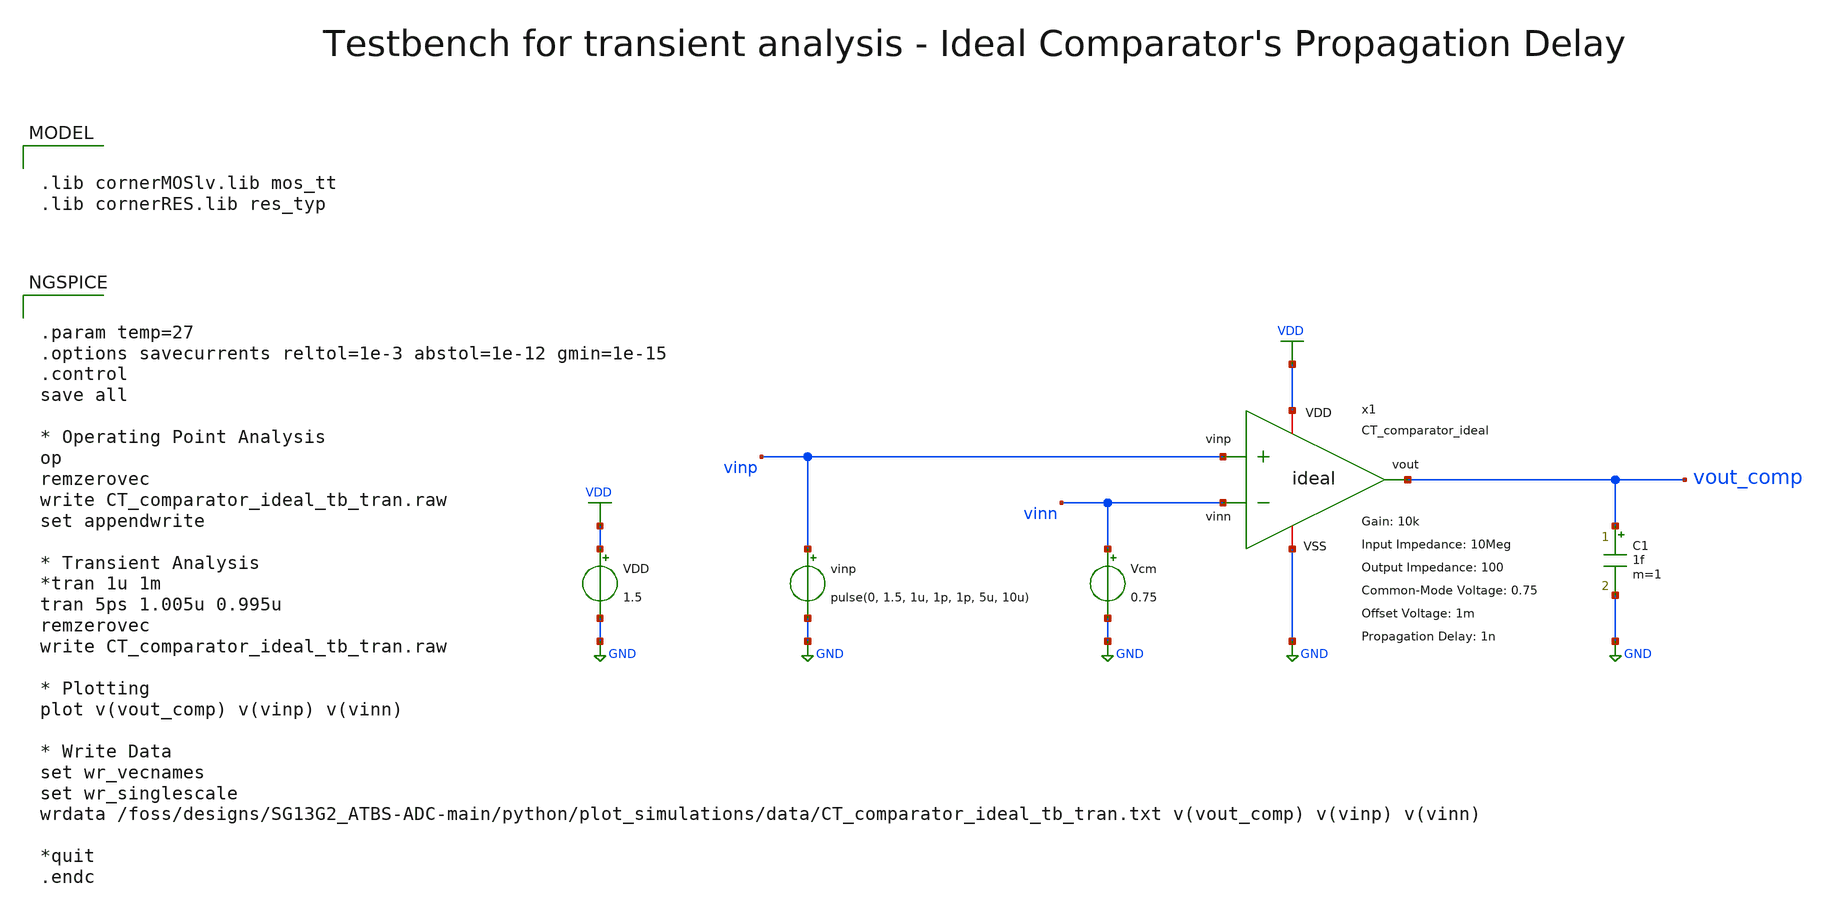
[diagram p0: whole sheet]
** sch_path: SG13G2_ATBS-ADC-main/xschem/comparator/continuous_time/ideal/testbenches/CT_comparator_ideal_tb_tran.sch
**.subckt CT_comparator_ideal_tb_tran
C1 vout_comp GND 1f m=1
Vcm vinn GND 0.75
vinp vinp GND pulse(0, 1.5, 1u, 1p, 1p, 5u, 10u)
VDD VDD GND 1.5
x1 vinp vinn VDD vout_comp GND CT_comparator_ideal A=10k Rin=10Meg Rout=100 Pdc=3.5u Vcm=0.75
+ Voffs=1m tpd=1n
**** begin user architecture code

.lib cornerMOSlv.lib mos_tt
.lib cornerRES.lib res_typ



.param temp=27
.options savecurrents reltol=1e-3 abstol=1e-12 gmin=1e-15
.control
save all

* Operating Point Analysis
op
remzerovec
write CT_comparator_ideal_tb_tran.raw
set appendwrite

* Transient Analysis
*tran 1u 1m
tran 5ps 1.005u 0.995u
remzerovec
write CT_comparator_ideal_tb_tran.raw

* Plotting
plot v(vout_comp) v(vinp) v(vinn)

* Write Data
set wr_vecnames
set wr_singlescale
wrdata
+ /foss/designs/SG13G2_ATBS-ADC-main/python/plot_simulations/data/CT_comparator_ideal_tb_tran.txt v(vout_comp) v(vinp) v(vinn)

*quit
.endc

**** end user architecture code
**.ends

* expanding   symbol:  comparator/continuous_time/ideal/CT_comparator_ideal.sym # of pins=5
** sym_path: SG13G2_ATBS-ADC-main/xschem/comparator/continuous_time/ideal/CT_comparator_ideal.sym
** sch_path: SG13G2_ATBS-ADC-main/xschem/comparator/continuous_time/ideal/CT_comparator_ideal.sch
.subckt CT_comparator_ideal vinp vinn VDD vout VSS  A=10k Rin=10Meg Rout=100 Vcm=0.75 Voffs=1m
+ tpd=1n
*.ipin vinn
*.opin vout
*.ipin vinp
*.iopin VSS
*.iopin VDD
R1 vinp vinn {Rin} m=1
B1 net1 VSS v=v(VDD)/2*tanh({A}/(v(VDD)/2)*(v(vinp)-v(vinn)-{Voffs}))+{Vcm}
R3 net2 vout {Rout} m=1
A1 net1 net2 VSS del_subckt
.model del_subckt delay(delay=tpd buffer_size=8192)
.ends

.GLOBAL VDD
.GLOBAL GND
.end
